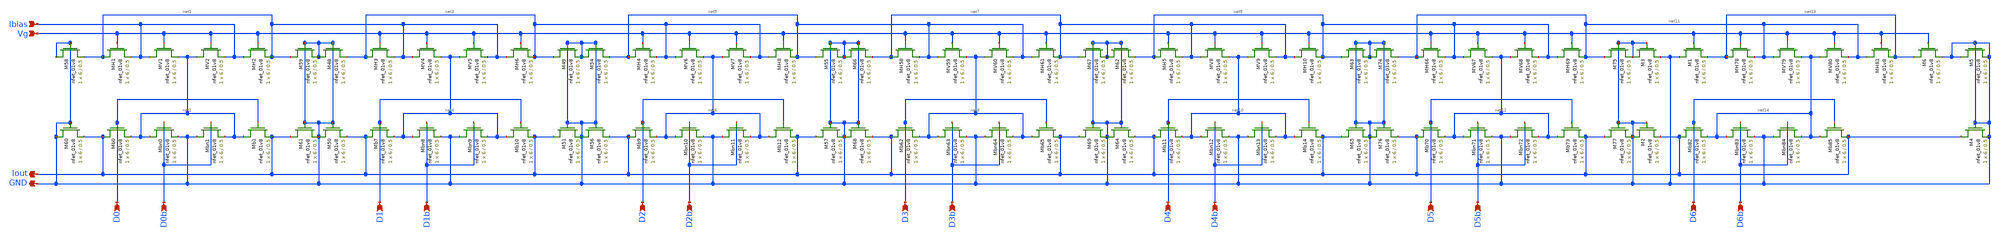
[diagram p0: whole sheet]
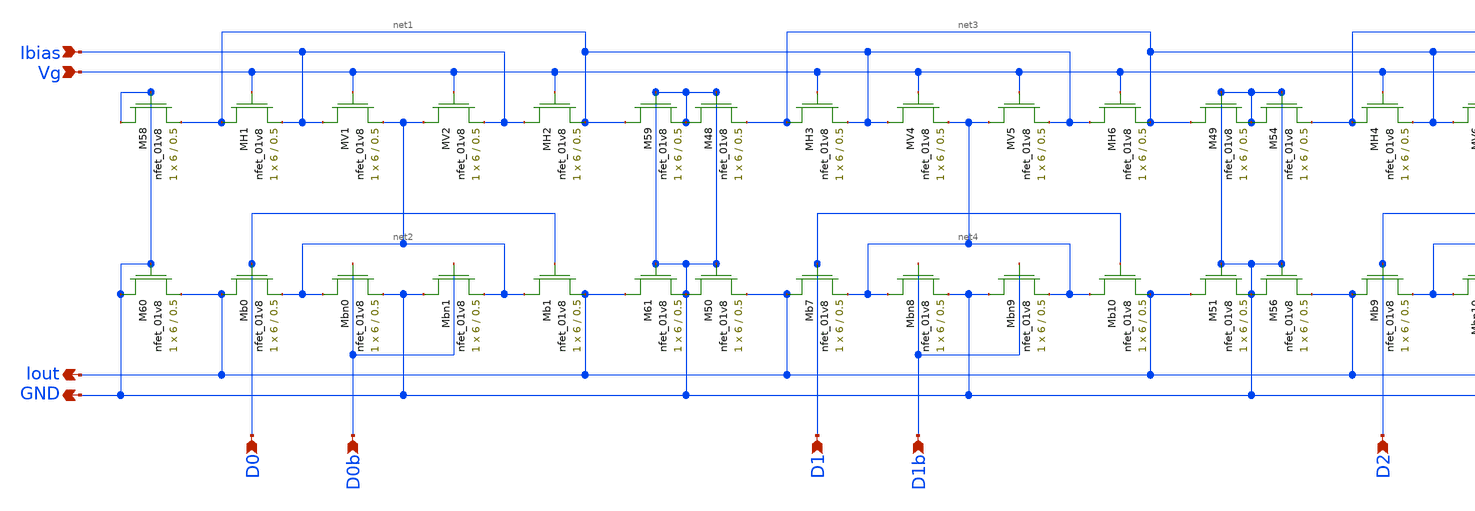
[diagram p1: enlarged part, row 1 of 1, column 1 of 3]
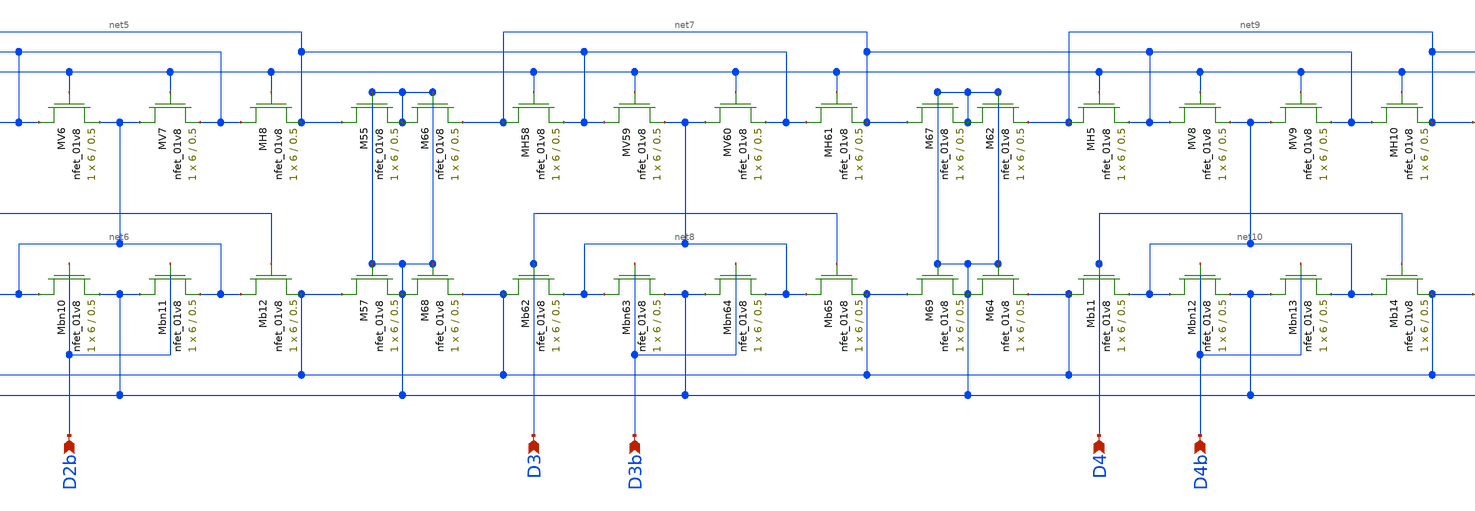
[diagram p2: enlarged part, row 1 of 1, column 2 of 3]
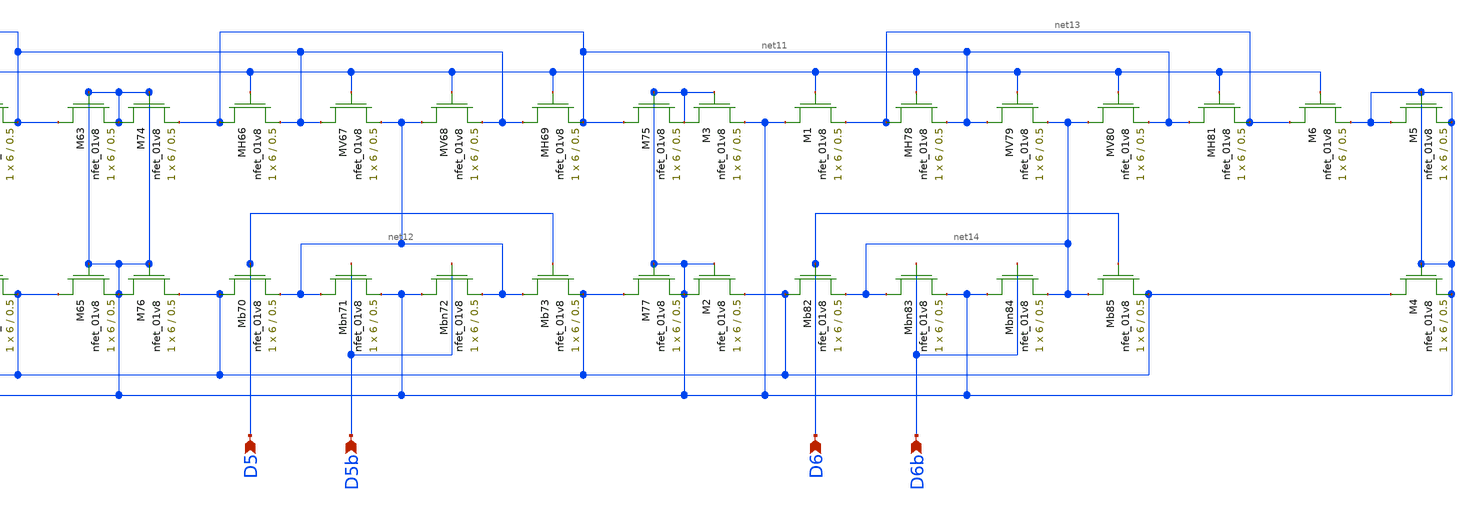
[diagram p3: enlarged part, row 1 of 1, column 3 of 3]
** sch_path: schematics/ieee DAC/Layout_Driven/LDS_ieee_DAC.sch
**.subckt LDS_ieee_DAC D0 D0b GND Iout Vg D1 D1b Ibias D2 D2b D3 D3b D4 D4b D5 D5b D6 D6b
*.ipin D0
*.ipin D0b
*.opin GND
*.opin Iout
*.ipin Vg
*.ipin D1
*.ipin D1b
*.ipin Ibias
*.ipin D2
*.ipin D2b
*.ipin D3
*.ipin D3b
*.ipin D4
*.ipin D4b
*.ipin D5
*.ipin D5b
*.ipin D6
*.ipin D6b
XMH1 net1 Vg Ibias GND sky130_fd_pr__nfet_01v8 L=0.5 W=6 nf=1 ad='int((nf+1)/2) * W/nf * 0.29' as='int((nf+2)/2) * W/nf * 0.29'
+ pd='2*int((nf+1)/2) * (W/nf + 0.29)' ps='2*int((nf+2)/2) * (W/nf + 0.29)' nrd='0.29 / W' nrs='0.29 / W'
+ sa=0 sb=0 sd=0 mult=1 m=1
XMV1 Ibias Vg net2 GND sky130_fd_pr__nfet_01v8 L=0.5 W=6 nf=1 ad='int((nf+1)/2) * W/nf * 0.29' as='int((nf+2)/2) * W/nf * 0.29'
+ pd='2*int((nf+1)/2) * (W/nf + 0.29)' ps='2*int((nf+2)/2) * (W/nf + 0.29)' nrd='0.29 / W' nrs='0.29 / W'
+ sa=0 sb=0 sd=0 mult=1 m=1
XMV2 net2 Vg Ibias GND sky130_fd_pr__nfet_01v8 L=0.5 W=6 nf=1 ad='int((nf+1)/2) * W/nf * 0.29' as='int((nf+2)/2) * W/nf * 0.29'
+ pd='2*int((nf+1)/2) * (W/nf + 0.29)' ps='2*int((nf+2)/2) * (W/nf + 0.29)' nrd='0.29 / W' nrs='0.29 / W'
+ sa=0 sb=0 sd=0 mult=1 m=1
XMH2 Ibias Vg net1 GND sky130_fd_pr__nfet_01v8 L=0.5 W=6 nf=1 ad='int((nf+1)/2) * W/nf * 0.29' as='int((nf+2)/2) * W/nf * 0.29'
+ pd='2*int((nf+1)/2) * (W/nf + 0.29)' ps='2*int((nf+2)/2) * (W/nf + 0.29)' nrd='0.29 / W' nrs='0.29 / W'
+ sa=0 sb=0 sd=0 mult=1 m=1
XMb0 Iout D0 net2 GND sky130_fd_pr__nfet_01v8 L=0.5 W=6 nf=1 ad='int((nf+1)/2) * W/nf * 0.29' as='int((nf+2)/2) * W/nf * 0.29'
+ pd='2*int((nf+1)/2) * (W/nf + 0.29)' ps='2*int((nf+2)/2) * (W/nf + 0.29)' nrd='0.29 / W' nrs='0.29 / W'
+ sa=0 sb=0 sd=0 mult=1 m=1
XMbn0 net2 D0b GND GND sky130_fd_pr__nfet_01v8 L=0.5 W=6 nf=1 ad='int((nf+1)/2) * W/nf * 0.29' as='int((nf+2)/2) * W/nf * 0.29'
+ pd='2*int((nf+1)/2) * (W/nf + 0.29)' ps='2*int((nf+2)/2) * (W/nf + 0.29)' nrd='0.29 / W' nrs='0.29 / W'
+ sa=0 sb=0 sd=0 mult=1 m=1
XMbn1 GND D0b net2 GND sky130_fd_pr__nfet_01v8 L=0.5 W=6 nf=1 ad='int((nf+1)/2) * W/nf * 0.29' as='int((nf+2)/2) * W/nf * 0.29'
+ pd='2*int((nf+1)/2) * (W/nf + 0.29)' ps='2*int((nf+2)/2) * (W/nf + 0.29)' nrd='0.29 / W' nrs='0.29 / W'
+ sa=0 sb=0 sd=0 mult=1 m=1
XMb1 net2 D0 Iout GND sky130_fd_pr__nfet_01v8 L=0.5 W=6 nf=1 ad='int((nf+1)/2) * W/nf * 0.29' as='int((nf+2)/2) * W/nf * 0.29'
+ pd='2*int((nf+1)/2) * (W/nf + 0.29)' ps='2*int((nf+2)/2) * (W/nf + 0.29)' nrd='0.29 / W' nrs='0.29 / W'
+ sa=0 sb=0 sd=0 mult=1 m=1
XM58 GND GND net1 GND sky130_fd_pr__nfet_01v8 L=0.5 W=6 nf=1 ad='int((nf+1)/2) * W/nf * 0.29' as='int((nf+2)/2) * W/nf * 0.29'
+ pd='2*int((nf+1)/2) * (W/nf + 0.29)' ps='2*int((nf+2)/2) * (W/nf + 0.29)' nrd='0.29 / W' nrs='0.29 / W'
+ sa=0 sb=0 sd=0 mult=1 m=1
XM59 net1 GND GND GND sky130_fd_pr__nfet_01v8 L=0.5 W=6 nf=1 ad='int((nf+1)/2) * W/nf * 0.29' as='int((nf+2)/2) * W/nf * 0.29'
+ pd='2*int((nf+1)/2) * (W/nf + 0.29)' ps='2*int((nf+2)/2) * (W/nf + 0.29)' nrd='0.29 / W' nrs='0.29 / W'
+ sa=0 sb=0 sd=0 mult=1 m=1
XM60 GND GND Iout GND sky130_fd_pr__nfet_01v8 L=0.5 W=6 nf=1 ad='int((nf+1)/2) * W/nf * 0.29' as='int((nf+2)/2) * W/nf * 0.29'
+ pd='2*int((nf+1)/2) * (W/nf + 0.29)' ps='2*int((nf+2)/2) * (W/nf + 0.29)' nrd='0.29 / W' nrs='0.29 / W'
+ sa=0 sb=0 sd=0 mult=1 m=1
XM61 Iout GND GND GND sky130_fd_pr__nfet_01v8 L=0.5 W=6 nf=1 ad='int((nf+1)/2) * W/nf * 0.29' as='int((nf+2)/2) * W/nf * 0.29'
+ pd='2*int((nf+1)/2) * (W/nf + 0.29)' ps='2*int((nf+2)/2) * (W/nf + 0.29)' nrd='0.29 / W' nrs='0.29 / W'
+ sa=0 sb=0 sd=0 mult=1 m=1
XMH3 net3 Vg net1 GND sky130_fd_pr__nfet_01v8 L=0.5 W=6 nf=1 ad='int((nf+1)/2) * W/nf * 0.29' as='int((nf+2)/2) * W/nf * 0.29'
+ pd='2*int((nf+1)/2) * (W/nf + 0.29)' ps='2*int((nf+2)/2) * (W/nf + 0.29)' nrd='0.29 / W' nrs='0.29 / W'
+ sa=0 sb=0 sd=0 mult=1 m=1
XMV4 net1 Vg net4 GND sky130_fd_pr__nfet_01v8 L=0.5 W=6 nf=1 ad='int((nf+1)/2) * W/nf * 0.29' as='int((nf+2)/2) * W/nf * 0.29'
+ pd='2*int((nf+1)/2) * (W/nf + 0.29)' ps='2*int((nf+2)/2) * (W/nf + 0.29)' nrd='0.29 / W' nrs='0.29 / W'
+ sa=0 sb=0 sd=0 mult=1 m=1
XMV5 net4 Vg net1 GND sky130_fd_pr__nfet_01v8 L=0.5 W=6 nf=1 ad='int((nf+1)/2) * W/nf * 0.29' as='int((nf+2)/2) * W/nf * 0.29'
+ pd='2*int((nf+1)/2) * (W/nf + 0.29)' ps='2*int((nf+2)/2) * (W/nf + 0.29)' nrd='0.29 / W' nrs='0.29 / W'
+ sa=0 sb=0 sd=0 mult=1 m=1
XMH6 net1 Vg net3 GND sky130_fd_pr__nfet_01v8 L=0.5 W=6 nf=1 ad='int((nf+1)/2) * W/nf * 0.29' as='int((nf+2)/2) * W/nf * 0.29'
+ pd='2*int((nf+1)/2) * (W/nf + 0.29)' ps='2*int((nf+2)/2) * (W/nf + 0.29)' nrd='0.29 / W' nrs='0.29 / W'
+ sa=0 sb=0 sd=0 mult=1 m=1
XMb7 Iout D1 net4 GND sky130_fd_pr__nfet_01v8 L=0.5 W=6 nf=1 ad='int((nf+1)/2) * W/nf * 0.29' as='int((nf+2)/2) * W/nf * 0.29'
+ pd='2*int((nf+1)/2) * (W/nf + 0.29)' ps='2*int((nf+2)/2) * (W/nf + 0.29)' nrd='0.29 / W' nrs='0.29 / W'
+ sa=0 sb=0 sd=0 mult=1 m=1
XMbn8 net4 D1b GND GND sky130_fd_pr__nfet_01v8 L=0.5 W=6 nf=1 ad='int((nf+1)/2) * W/nf * 0.29' as='int((nf+2)/2) * W/nf * 0.29'
+ pd='2*int((nf+1)/2) * (W/nf + 0.29)' ps='2*int((nf+2)/2) * (W/nf + 0.29)' nrd='0.29 / W' nrs='0.29 / W'
+ sa=0 sb=0 sd=0 mult=1 m=1
XMbn9 GND D1b net4 GND sky130_fd_pr__nfet_01v8 L=0.5 W=6 nf=1 ad='int((nf+1)/2) * W/nf * 0.29' as='int((nf+2)/2) * W/nf * 0.29'
+ pd='2*int((nf+1)/2) * (W/nf + 0.29)' ps='2*int((nf+2)/2) * (W/nf + 0.29)' nrd='0.29 / W' nrs='0.29 / W'
+ sa=0 sb=0 sd=0 mult=1 m=1
XMb10 net4 D1 Iout GND sky130_fd_pr__nfet_01v8 L=0.5 W=6 nf=1 ad='int((nf+1)/2) * W/nf * 0.29' as='int((nf+2)/2) * W/nf * 0.29'
+ pd='2*int((nf+1)/2) * (W/nf + 0.29)' ps='2*int((nf+2)/2) * (W/nf + 0.29)' nrd='0.29 / W' nrs='0.29 / W'
+ sa=0 sb=0 sd=0 mult=1 m=1
XM48 GND GND net3 GND sky130_fd_pr__nfet_01v8 L=0.5 W=6 nf=1 ad='int((nf+1)/2) * W/nf * 0.29' as='int((nf+2)/2) * W/nf * 0.29'
+ pd='2*int((nf+1)/2) * (W/nf + 0.29)' ps='2*int((nf+2)/2) * (W/nf + 0.29)' nrd='0.29 / W' nrs='0.29 / W'
+ sa=0 sb=0 sd=0 mult=1 m=1
XM49 net3 GND GND GND sky130_fd_pr__nfet_01v8 L=0.5 W=6 nf=1 ad='int((nf+1)/2) * W/nf * 0.29' as='int((nf+2)/2) * W/nf * 0.29'
+ pd='2*int((nf+1)/2) * (W/nf + 0.29)' ps='2*int((nf+2)/2) * (W/nf + 0.29)' nrd='0.29 / W' nrs='0.29 / W'
+ sa=0 sb=0 sd=0 mult=1 m=1
XM50 GND GND Iout GND sky130_fd_pr__nfet_01v8 L=0.5 W=6 nf=1 ad='int((nf+1)/2) * W/nf * 0.29' as='int((nf+2)/2) * W/nf * 0.29'
+ pd='2*int((nf+1)/2) * (W/nf + 0.29)' ps='2*int((nf+2)/2) * (W/nf + 0.29)' nrd='0.29 / W' nrs='0.29 / W'
+ sa=0 sb=0 sd=0 mult=1 m=1
XM51 Iout GND GND GND sky130_fd_pr__nfet_01v8 L=0.5 W=6 nf=1 ad='int((nf+1)/2) * W/nf * 0.29' as='int((nf+2)/2) * W/nf * 0.29'
+ pd='2*int((nf+1)/2) * (W/nf + 0.29)' ps='2*int((nf+2)/2) * (W/nf + 0.29)' nrd='0.29 / W' nrs='0.29 / W'
+ sa=0 sb=0 sd=0 mult=1 m=1
XMH4 net5 Vg net3 GND sky130_fd_pr__nfet_01v8 L=0.5 W=6 nf=1 ad='int((nf+1)/2) * W/nf * 0.29' as='int((nf+2)/2) * W/nf * 0.29'
+ pd='2*int((nf+1)/2) * (W/nf + 0.29)' ps='2*int((nf+2)/2) * (W/nf + 0.29)' nrd='0.29 / W' nrs='0.29 / W'
+ sa=0 sb=0 sd=0 mult=1 m=1
XMV6 net3 Vg net6 GND sky130_fd_pr__nfet_01v8 L=0.5 W=6 nf=1 ad='int((nf+1)/2) * W/nf * 0.29' as='int((nf+2)/2) * W/nf * 0.29'
+ pd='2*int((nf+1)/2) * (W/nf + 0.29)' ps='2*int((nf+2)/2) * (W/nf + 0.29)' nrd='0.29 / W' nrs='0.29 / W'
+ sa=0 sb=0 sd=0 mult=1 m=1
XMV7 net6 Vg net3 GND sky130_fd_pr__nfet_01v8 L=0.5 W=6 nf=1 ad='int((nf+1)/2) * W/nf * 0.29' as='int((nf+2)/2) * W/nf * 0.29'
+ pd='2*int((nf+1)/2) * (W/nf + 0.29)' ps='2*int((nf+2)/2) * (W/nf + 0.29)' nrd='0.29 / W' nrs='0.29 / W'
+ sa=0 sb=0 sd=0 mult=1 m=1
XMH8 net3 Vg net5 GND sky130_fd_pr__nfet_01v8 L=0.5 W=6 nf=1 ad='int((nf+1)/2) * W/nf * 0.29' as='int((nf+2)/2) * W/nf * 0.29'
+ pd='2*int((nf+1)/2) * (W/nf + 0.29)' ps='2*int((nf+2)/2) * (W/nf + 0.29)' nrd='0.29 / W' nrs='0.29 / W'
+ sa=0 sb=0 sd=0 mult=1 m=1
XMb9 Iout D2 net6 GND sky130_fd_pr__nfet_01v8 L=0.5 W=6 nf=1 ad='int((nf+1)/2) * W/nf * 0.29' as='int((nf+2)/2) * W/nf * 0.29'
+ pd='2*int((nf+1)/2) * (W/nf + 0.29)' ps='2*int((nf+2)/2) * (W/nf + 0.29)' nrd='0.29 / W' nrs='0.29 / W'
+ sa=0 sb=0 sd=0 mult=1 m=1
XMbn10 net6 D2b GND GND sky130_fd_pr__nfet_01v8 L=0.5 W=6 nf=1 ad='int((nf+1)/2) * W/nf * 0.29' as='int((nf+2)/2) * W/nf * 0.29'
+ pd='2*int((nf+1)/2) * (W/nf + 0.29)' ps='2*int((nf+2)/2) * (W/nf + 0.29)' nrd='0.29 / W' nrs='0.29 / W'
+ sa=0 sb=0 sd=0 mult=1 m=1
XMbn11 GND D2b net6 GND sky130_fd_pr__nfet_01v8 L=0.5 W=6 nf=1 ad='int((nf+1)/2) * W/nf * 0.29' as='int((nf+2)/2) * W/nf * 0.29'
+ pd='2*int((nf+1)/2) * (W/nf + 0.29)' ps='2*int((nf+2)/2) * (W/nf + 0.29)' nrd='0.29 / W' nrs='0.29 / W'
+ sa=0 sb=0 sd=0 mult=1 m=1
XMb12 net6 D2 Iout GND sky130_fd_pr__nfet_01v8 L=0.5 W=6 nf=1 ad='int((nf+1)/2) * W/nf * 0.29' as='int((nf+2)/2) * W/nf * 0.29'
+ pd='2*int((nf+1)/2) * (W/nf + 0.29)' ps='2*int((nf+2)/2) * (W/nf + 0.29)' nrd='0.29 / W' nrs='0.29 / W'
+ sa=0 sb=0 sd=0 mult=1 m=1
XM54 GND GND net5 GND sky130_fd_pr__nfet_01v8 L=0.5 W=6 nf=1 ad='int((nf+1)/2) * W/nf * 0.29' as='int((nf+2)/2) * W/nf * 0.29'
+ pd='2*int((nf+1)/2) * (W/nf + 0.29)' ps='2*int((nf+2)/2) * (W/nf + 0.29)' nrd='0.29 / W' nrs='0.29 / W'
+ sa=0 sb=0 sd=0 mult=1 m=1
XM55 net5 GND GND GND sky130_fd_pr__nfet_01v8 L=0.5 W=6 nf=1 ad='int((nf+1)/2) * W/nf * 0.29' as='int((nf+2)/2) * W/nf * 0.29'
+ pd='2*int((nf+1)/2) * (W/nf + 0.29)' ps='2*int((nf+2)/2) * (W/nf + 0.29)' nrd='0.29 / W' nrs='0.29 / W'
+ sa=0 sb=0 sd=0 mult=1 m=1
XM56 GND GND Iout GND sky130_fd_pr__nfet_01v8 L=0.5 W=6 nf=1 ad='int((nf+1)/2) * W/nf * 0.29' as='int((nf+2)/2) * W/nf * 0.29'
+ pd='2*int((nf+1)/2) * (W/nf + 0.29)' ps='2*int((nf+2)/2) * (W/nf + 0.29)' nrd='0.29 / W' nrs='0.29 / W'
+ sa=0 sb=0 sd=0 mult=1 m=1
XM57 Iout GND GND GND sky130_fd_pr__nfet_01v8 L=0.5 W=6 nf=1 ad='int((nf+1)/2) * W/nf * 0.29' as='int((nf+2)/2) * W/nf * 0.29'
+ pd='2*int((nf+1)/2) * (W/nf + 0.29)' ps='2*int((nf+2)/2) * (W/nf + 0.29)' nrd='0.29 / W' nrs='0.29 / W'
+ sa=0 sb=0 sd=0 mult=1 m=1
XMH58 net7 Vg net5 GND sky130_fd_pr__nfet_01v8 L=0.5 W=6 nf=1 ad='int((nf+1)/2) * W/nf * 0.29' as='int((nf+2)/2) * W/nf * 0.29'
+ pd='2*int((nf+1)/2) * (W/nf + 0.29)' ps='2*int((nf+2)/2) * (W/nf + 0.29)' nrd='0.29 / W' nrs='0.29 / W'
+ sa=0 sb=0 sd=0 mult=1 m=1
XMV59 net5 Vg net8 GND sky130_fd_pr__nfet_01v8 L=0.5 W=6 nf=1 ad='int((nf+1)/2) * W/nf * 0.29' as='int((nf+2)/2) * W/nf * 0.29'
+ pd='2*int((nf+1)/2) * (W/nf + 0.29)' ps='2*int((nf+2)/2) * (W/nf + 0.29)' nrd='0.29 / W' nrs='0.29 / W'
+ sa=0 sb=0 sd=0 mult=1 m=1
XMV60 net8 Vg net5 GND sky130_fd_pr__nfet_01v8 L=0.5 W=6 nf=1 ad='int((nf+1)/2) * W/nf * 0.29' as='int((nf+2)/2) * W/nf * 0.29'
+ pd='2*int((nf+1)/2) * (W/nf + 0.29)' ps='2*int((nf+2)/2) * (W/nf + 0.29)' nrd='0.29 / W' nrs='0.29 / W'
+ sa=0 sb=0 sd=0 mult=1 m=1
XMH61 net5 Vg net7 GND sky130_fd_pr__nfet_01v8 L=0.5 W=6 nf=1 ad='int((nf+1)/2) * W/nf * 0.29' as='int((nf+2)/2) * W/nf * 0.29'
+ pd='2*int((nf+1)/2) * (W/nf + 0.29)' ps='2*int((nf+2)/2) * (W/nf + 0.29)' nrd='0.29 / W' nrs='0.29 / W'
+ sa=0 sb=0 sd=0 mult=1 m=1
XMb62 Iout D3 net8 GND sky130_fd_pr__nfet_01v8 L=0.5 W=6 nf=1 ad='int((nf+1)/2) * W/nf * 0.29' as='int((nf+2)/2) * W/nf * 0.29'
+ pd='2*int((nf+1)/2) * (W/nf + 0.29)' ps='2*int((nf+2)/2) * (W/nf + 0.29)' nrd='0.29 / W' nrs='0.29 / W'
+ sa=0 sb=0 sd=0 mult=1 m=1
XMbn63 net8 D3b GND GND sky130_fd_pr__nfet_01v8 L=0.5 W=6 nf=1 ad='int((nf+1)/2) * W/nf * 0.29' as='int((nf+2)/2) * W/nf * 0.29'
+ pd='2*int((nf+1)/2) * (W/nf + 0.29)' ps='2*int((nf+2)/2) * (W/nf + 0.29)' nrd='0.29 / W' nrs='0.29 / W'
+ sa=0 sb=0 sd=0 mult=1 m=1
XMbn64 GND D3b net8 GND sky130_fd_pr__nfet_01v8 L=0.5 W=6 nf=1 ad='int((nf+1)/2) * W/nf * 0.29' as='int((nf+2)/2) * W/nf * 0.29'
+ pd='2*int((nf+1)/2) * (W/nf + 0.29)' ps='2*int((nf+2)/2) * (W/nf + 0.29)' nrd='0.29 / W' nrs='0.29 / W'
+ sa=0 sb=0 sd=0 mult=1 m=1
XMb65 net8 D3 Iout GND sky130_fd_pr__nfet_01v8 L=0.5 W=6 nf=1 ad='int((nf+1)/2) * W/nf * 0.29' as='int((nf+2)/2) * W/nf * 0.29'
+ pd='2*int((nf+1)/2) * (W/nf + 0.29)' ps='2*int((nf+2)/2) * (W/nf + 0.29)' nrd='0.29 / W' nrs='0.29 / W'
+ sa=0 sb=0 sd=0 mult=1 m=1
XM66 GND GND net7 GND sky130_fd_pr__nfet_01v8 L=0.5 W=6 nf=1 ad='int((nf+1)/2) * W/nf * 0.29' as='int((nf+2)/2) * W/nf * 0.29'
+ pd='2*int((nf+1)/2) * (W/nf + 0.29)' ps='2*int((nf+2)/2) * (W/nf + 0.29)' nrd='0.29 / W' nrs='0.29 / W'
+ sa=0 sb=0 sd=0 mult=1 m=1
XM67 net7 GND GND GND sky130_fd_pr__nfet_01v8 L=0.5 W=6 nf=1 ad='int((nf+1)/2) * W/nf * 0.29' as='int((nf+2)/2) * W/nf * 0.29'
+ pd='2*int((nf+1)/2) * (W/nf + 0.29)' ps='2*int((nf+2)/2) * (W/nf + 0.29)' nrd='0.29 / W' nrs='0.29 / W'
+ sa=0 sb=0 sd=0 mult=1 m=1
XM68 GND GND Iout GND sky130_fd_pr__nfet_01v8 L=0.5 W=6 nf=1 ad='int((nf+1)/2) * W/nf * 0.29' as='int((nf+2)/2) * W/nf * 0.29'
+ pd='2*int((nf+1)/2) * (W/nf + 0.29)' ps='2*int((nf+2)/2) * (W/nf + 0.29)' nrd='0.29 / W' nrs='0.29 / W'
+ sa=0 sb=0 sd=0 mult=1 m=1
XM69 Iout GND GND GND sky130_fd_pr__nfet_01v8 L=0.5 W=6 nf=1 ad='int((nf+1)/2) * W/nf * 0.29' as='int((nf+2)/2) * W/nf * 0.29'
+ pd='2*int((nf+1)/2) * (W/nf + 0.29)' ps='2*int((nf+2)/2) * (W/nf + 0.29)' nrd='0.29 / W' nrs='0.29 / W'
+ sa=0 sb=0 sd=0 mult=1 m=1
XMH5 net9 Vg net7 GND sky130_fd_pr__nfet_01v8 L=0.5 W=6 nf=1 ad='int((nf+1)/2) * W/nf * 0.29' as='int((nf+2)/2) * W/nf * 0.29'
+ pd='2*int((nf+1)/2) * (W/nf + 0.29)' ps='2*int((nf+2)/2) * (W/nf + 0.29)' nrd='0.29 / W' nrs='0.29 / W'
+ sa=0 sb=0 sd=0 mult=1 m=1
XMV8 net7 Vg net10 GND sky130_fd_pr__nfet_01v8 L=0.5 W=6 nf=1 ad='int((nf+1)/2) * W/nf * 0.29' as='int((nf+2)/2) * W/nf * 0.29'
+ pd='2*int((nf+1)/2) * (W/nf + 0.29)' ps='2*int((nf+2)/2) * (W/nf + 0.29)' nrd='0.29 / W' nrs='0.29 / W'
+ sa=0 sb=0 sd=0 mult=1 m=1
XMV9 net10 Vg net7 GND sky130_fd_pr__nfet_01v8 L=0.5 W=6 nf=1 ad='int((nf+1)/2) * W/nf * 0.29' as='int((nf+2)/2) * W/nf * 0.29'
+ pd='2*int((nf+1)/2) * (W/nf + 0.29)' ps='2*int((nf+2)/2) * (W/nf + 0.29)' nrd='0.29 / W' nrs='0.29 / W'
+ sa=0 sb=0 sd=0 mult=1 m=1
XMH10 net7 Vg net9 GND sky130_fd_pr__nfet_01v8 L=0.5 W=6 nf=1 ad='int((nf+1)/2) * W/nf * 0.29' as='int((nf+2)/2) * W/nf * 0.29'
+ pd='2*int((nf+1)/2) * (W/nf + 0.29)' ps='2*int((nf+2)/2) * (W/nf + 0.29)' nrd='0.29 / W' nrs='0.29 / W'
+ sa=0 sb=0 sd=0 mult=1 m=1
XMb11 Iout D4 net10 GND sky130_fd_pr__nfet_01v8 L=0.5 W=6 nf=1 ad='int((nf+1)/2) * W/nf * 0.29' as='int((nf+2)/2) * W/nf * 0.29'
+ pd='2*int((nf+1)/2) * (W/nf + 0.29)' ps='2*int((nf+2)/2) * (W/nf + 0.29)' nrd='0.29 / W' nrs='0.29 / W'
+ sa=0 sb=0 sd=0 mult=1 m=1
XMbn12 net10 D4b GND GND sky130_fd_pr__nfet_01v8 L=0.5 W=6 nf=1 ad='int((nf+1)/2) * W/nf * 0.29' as='int((nf+2)/2) * W/nf * 0.29'
+ pd='2*int((nf+1)/2) * (W/nf + 0.29)' ps='2*int((nf+2)/2) * (W/nf + 0.29)' nrd='0.29 / W' nrs='0.29 / W'
+ sa=0 sb=0 sd=0 mult=1 m=1
XMbn13 GND D4b net10 GND sky130_fd_pr__nfet_01v8 L=0.5 W=6 nf=1 ad='int((nf+1)/2) * W/nf * 0.29' as='int((nf+2)/2) * W/nf * 0.29'
+ pd='2*int((nf+1)/2) * (W/nf + 0.29)' ps='2*int((nf+2)/2) * (W/nf + 0.29)' nrd='0.29 / W' nrs='0.29 / W'
+ sa=0 sb=0 sd=0 mult=1 m=1
XMb14 net10 D4 Iout GND sky130_fd_pr__nfet_01v8 L=0.5 W=6 nf=1 ad='int((nf+1)/2) * W/nf * 0.29' as='int((nf+2)/2) * W/nf * 0.29'
+ pd='2*int((nf+1)/2) * (W/nf + 0.29)' ps='2*int((nf+2)/2) * (W/nf + 0.29)' nrd='0.29 / W' nrs='0.29 / W'
+ sa=0 sb=0 sd=0 mult=1 m=1
XM62 GND GND net9 GND sky130_fd_pr__nfet_01v8 L=0.5 W=6 nf=1 ad='int((nf+1)/2) * W/nf * 0.29' as='int((nf+2)/2) * W/nf * 0.29'
+ pd='2*int((nf+1)/2) * (W/nf + 0.29)' ps='2*int((nf+2)/2) * (W/nf + 0.29)' nrd='0.29 / W' nrs='0.29 / W'
+ sa=0 sb=0 sd=0 mult=1 m=1
XM63 net9 GND GND GND sky130_fd_pr__nfet_01v8 L=0.5 W=6 nf=1 ad='int((nf+1)/2) * W/nf * 0.29' as='int((nf+2)/2) * W/nf * 0.29'
+ pd='2*int((nf+1)/2) * (W/nf + 0.29)' ps='2*int((nf+2)/2) * (W/nf + 0.29)' nrd='0.29 / W' nrs='0.29 / W'
+ sa=0 sb=0 sd=0 mult=1 m=1
XM64 GND GND Iout GND sky130_fd_pr__nfet_01v8 L=0.5 W=6 nf=1 ad='int((nf+1)/2) * W/nf * 0.29' as='int((nf+2)/2) * W/nf * 0.29'
+ pd='2*int((nf+1)/2) * (W/nf + 0.29)' ps='2*int((nf+2)/2) * (W/nf + 0.29)' nrd='0.29 / W' nrs='0.29 / W'
+ sa=0 sb=0 sd=0 mult=1 m=1
XM65 Iout GND GND GND sky130_fd_pr__nfet_01v8 L=0.5 W=6 nf=1 ad='int((nf+1)/2) * W/nf * 0.29' as='int((nf+2)/2) * W/nf * 0.29'
+ pd='2*int((nf+1)/2) * (W/nf + 0.29)' ps='2*int((nf+2)/2) * (W/nf + 0.29)' nrd='0.29 / W' nrs='0.29 / W'
+ sa=0 sb=0 sd=0 mult=1 m=1
XMH66 net11 Vg net9 GND sky130_fd_pr__nfet_01v8 L=0.5 W=6 nf=1 ad='int((nf+1)/2) * W/nf * 0.29' as='int((nf+2)/2) * W/nf * 0.29'
+ pd='2*int((nf+1)/2) * (W/nf + 0.29)' ps='2*int((nf+2)/2) * (W/nf + 0.29)' nrd='0.29 / W' nrs='0.29 / W'
+ sa=0 sb=0 sd=0 mult=1 m=1
XMV67 net9 Vg net12 GND sky130_fd_pr__nfet_01v8 L=0.5 W=6 nf=1 ad='int((nf+1)/2) * W/nf * 0.29' as='int((nf+2)/2) * W/nf * 0.29'
+ pd='2*int((nf+1)/2) * (W/nf + 0.29)' ps='2*int((nf+2)/2) * (W/nf + 0.29)' nrd='0.29 / W' nrs='0.29 / W'
+ sa=0 sb=0 sd=0 mult=1 m=1
XMV68 net12 Vg net9 GND sky130_fd_pr__nfet_01v8 L=0.5 W=6 nf=1 ad='int((nf+1)/2) * W/nf * 0.29' as='int((nf+2)/2) * W/nf * 0.29'
+ pd='2*int((nf+1)/2) * (W/nf + 0.29)' ps='2*int((nf+2)/2) * (W/nf + 0.29)' nrd='0.29 / W' nrs='0.29 / W'
+ sa=0 sb=0 sd=0 mult=1 m=1
XMH69 net9 Vg net11 GND sky130_fd_pr__nfet_01v8 L=0.5 W=6 nf=1 ad='int((nf+1)/2) * W/nf * 0.29' as='int((nf+2)/2) * W/nf * 0.29'
+ pd='2*int((nf+1)/2) * (W/nf + 0.29)' ps='2*int((nf+2)/2) * (W/nf + 0.29)' nrd='0.29 / W' nrs='0.29 / W'
+ sa=0 sb=0 sd=0 mult=1 m=1
XMb70 Iout D5 net12 GND sky130_fd_pr__nfet_01v8 L=0.5 W=6 nf=1 ad='int((nf+1)/2) * W/nf * 0.29' as='int((nf+2)/2) * W/nf * 0.29'
+ pd='2*int((nf+1)/2) * (W/nf + 0.29)' ps='2*int((nf+2)/2) * (W/nf + 0.29)' nrd='0.29 / W' nrs='0.29 / W'
+ sa=0 sb=0 sd=0 mult=1 m=1
XMbn71 net12 D5b GND GND sky130_fd_pr__nfet_01v8 L=0.5 W=6 nf=1 ad='int((nf+1)/2) * W/nf * 0.29' as='int((nf+2)/2) * W/nf * 0.29'
+ pd='2*int((nf+1)/2) * (W/nf + 0.29)' ps='2*int((nf+2)/2) * (W/nf + 0.29)' nrd='0.29 / W' nrs='0.29 / W'
+ sa=0 sb=0 sd=0 mult=1 m=1
XMbn72 GND D5b net12 GND sky130_fd_pr__nfet_01v8 L=0.5 W=6 nf=1 ad='int((nf+1)/2) * W/nf * 0.29' as='int((nf+2)/2) * W/nf * 0.29'
+ pd='2*int((nf+1)/2) * (W/nf + 0.29)' ps='2*int((nf+2)/2) * (W/nf + 0.29)' nrd='0.29 / W' nrs='0.29 / W'
+ sa=0 sb=0 sd=0 mult=1 m=1
XMb73 net12 D5 Iout GND sky130_fd_pr__nfet_01v8 L=0.5 W=6 nf=1 ad='int((nf+1)/2) * W/nf * 0.29' as='int((nf+2)/2) * W/nf * 0.29'
+ pd='2*int((nf+1)/2) * (W/nf + 0.29)' ps='2*int((nf+2)/2) * (W/nf + 0.29)' nrd='0.29 / W' nrs='0.29 / W'
+ sa=0 sb=0 sd=0 mult=1 m=1
XM74 GND GND net11 GND sky130_fd_pr__nfet_01v8 L=0.5 W=6 nf=1 ad='int((nf+1)/2) * W/nf * 0.29' as='int((nf+2)/2) * W/nf * 0.29'
+ pd='2*int((nf+1)/2) * (W/nf + 0.29)' ps='2*int((nf+2)/2) * (W/nf + 0.29)' nrd='0.29 / W' nrs='0.29 / W'
+ sa=0 sb=0 sd=0 mult=1 m=1
XM75 net11 GND GND GND sky130_fd_pr__nfet_01v8 L=0.5 W=6 nf=1 ad='int((nf+1)/2) * W/nf * 0.29' as='int((nf+2)/2) * W/nf * 0.29'
+ pd='2*int((nf+1)/2) * (W/nf + 0.29)' ps='2*int((nf+2)/2) * (W/nf + 0.29)' nrd='0.29 / W' nrs='0.29 / W'
+ sa=0 sb=0 sd=0 mult=1 m=1
XM76 GND GND Iout GND sky130_fd_pr__nfet_01v8 L=0.5 W=6 nf=1 ad='int((nf+1)/2) * W/nf * 0.29' as='int((nf+2)/2) * W/nf * 0.29'
+ pd='2*int((nf+1)/2) * (W/nf + 0.29)' ps='2*int((nf+2)/2) * (W/nf + 0.29)' nrd='0.29 / W' nrs='0.29 / W'
+ sa=0 sb=0 sd=0 mult=1 m=1
XM77 Iout GND GND GND sky130_fd_pr__nfet_01v8 L=0.5 W=6 nf=1 ad='int((nf+1)/2) * W/nf * 0.29' as='int((nf+2)/2) * W/nf * 0.29'
+ pd='2*int((nf+1)/2) * (W/nf + 0.29)' ps='2*int((nf+2)/2) * (W/nf + 0.29)' nrd='0.29 / W' nrs='0.29 / W'
+ sa=0 sb=0 sd=0 mult=1 m=1
XMH78 net13 Vg net11 GND sky130_fd_pr__nfet_01v8 L=0.5 W=6 nf=1 ad='int((nf+1)/2) * W/nf * 0.29' as='int((nf+2)/2) * W/nf * 0.29'
+ pd='2*int((nf+1)/2) * (W/nf + 0.29)' ps='2*int((nf+2)/2) * (W/nf + 0.29)' nrd='0.29 / W' nrs='0.29 / W'
+ sa=0 sb=0 sd=0 mult=1 m=1
XMV79 net11 Vg net14 GND sky130_fd_pr__nfet_01v8 L=0.5 W=6 nf=1 ad='int((nf+1)/2) * W/nf * 0.29' as='int((nf+2)/2) * W/nf * 0.29'
+ pd='2*int((nf+1)/2) * (W/nf + 0.29)' ps='2*int((nf+2)/2) * (W/nf + 0.29)' nrd='0.29 / W' nrs='0.29 / W'
+ sa=0 sb=0 sd=0 mult=1 m=1
XMV80 net14 Vg net11 GND sky130_fd_pr__nfet_01v8 L=0.5 W=6 nf=1 ad='int((nf+1)/2) * W/nf * 0.29' as='int((nf+2)/2) * W/nf * 0.29'
+ pd='2*int((nf+1)/2) * (W/nf + 0.29)' ps='2*int((nf+2)/2) * (W/nf + 0.29)' nrd='0.29 / W' nrs='0.29 / W'
+ sa=0 sb=0 sd=0 mult=1 m=1
XMH81 net11 Vg net13 GND sky130_fd_pr__nfet_01v8 L=0.5 W=6 nf=1 ad='int((nf+1)/2) * W/nf * 0.29' as='int((nf+2)/2) * W/nf * 0.29'
+ pd='2*int((nf+1)/2) * (W/nf + 0.29)' ps='2*int((nf+2)/2) * (W/nf + 0.29)' nrd='0.29 / W' nrs='0.29 / W'
+ sa=0 sb=0 sd=0 mult=1 m=1
XMb82 Iout D6 net14 GND sky130_fd_pr__nfet_01v8 L=0.5 W=6 nf=1 ad='int((nf+1)/2) * W/nf * 0.29' as='int((nf+2)/2) * W/nf * 0.29'
+ pd='2*int((nf+1)/2) * (W/nf + 0.29)' ps='2*int((nf+2)/2) * (W/nf + 0.29)' nrd='0.29 / W' nrs='0.29 / W'
+ sa=0 sb=0 sd=0 mult=1 m=1
XMbn83 net14 D6b GND GND sky130_fd_pr__nfet_01v8 L=0.5 W=6 nf=1 ad='int((nf+1)/2) * W/nf * 0.29' as='int((nf+2)/2) * W/nf * 0.29'
+ pd='2*int((nf+1)/2) * (W/nf + 0.29)' ps='2*int((nf+2)/2) * (W/nf + 0.29)' nrd='0.29 / W' nrs='0.29 / W'
+ sa=0 sb=0 sd=0 mult=1 m=1
XMbn84 GND D6b net14 GND sky130_fd_pr__nfet_01v8 L=0.5 W=6 nf=1 ad='int((nf+1)/2) * W/nf * 0.29' as='int((nf+2)/2) * W/nf * 0.29'
+ pd='2*int((nf+1)/2) * (W/nf + 0.29)' ps='2*int((nf+2)/2) * (W/nf + 0.29)' nrd='0.29 / W' nrs='0.29 / W'
+ sa=0 sb=0 sd=0 mult=1 m=1
XMb85 net14 D6 Iout GND sky130_fd_pr__nfet_01v8 L=0.5 W=6 nf=1 ad='int((nf+1)/2) * W/nf * 0.29' as='int((nf+2)/2) * W/nf * 0.29'
+ pd='2*int((nf+1)/2) * (W/nf + 0.29)' ps='2*int((nf+2)/2) * (W/nf + 0.29)' nrd='0.29 / W' nrs='0.29 / W'
+ sa=0 sb=0 sd=0 mult=1 m=1
XM1 GND Vg net13 GND sky130_fd_pr__nfet_01v8 L=0.5 W=6 nf=1 ad='int((nf+1)/2) * W/nf * 0.29' as='int((nf+2)/2) * W/nf * 0.29'
+ pd='2*int((nf+1)/2) * (W/nf + 0.29)' ps='2*int((nf+2)/2) * (W/nf + 0.29)' nrd='0.29 / W' nrs='0.29 / W'
+ sa=0 sb=0 sd=0 mult=1 m=1
XM2 GND GND Iout GND sky130_fd_pr__nfet_01v8 L=0.5 W=6 nf=1 ad='int((nf+1)/2) * W/nf * 0.29' as='int((nf+2)/2) * W/nf * 0.29'
+ pd='2*int((nf+1)/2) * (W/nf + 0.29)' ps='2*int((nf+2)/2) * (W/nf + 0.29)' nrd='0.29 / W' nrs='0.29 / W'
+ sa=0 sb=0 sd=0 mult=1 m=1
XM4 Iout GND GND GND sky130_fd_pr__nfet_01v8 L=0.5 W=6 nf=1 ad='int((nf+1)/2) * W/nf * 0.29' as='int((nf+2)/2) * W/nf * 0.29'
+ pd='2*int((nf+1)/2) * (W/nf + 0.29)' ps='2*int((nf+2)/2) * (W/nf + 0.29)' nrd='0.29 / W' nrs='0.29 / W'
+ sa=0 sb=0 sd=0 mult=1 m=1
XM5 GND GND GND GND sky130_fd_pr__nfet_01v8 L=0.5 W=6 nf=1 ad='int((nf+1)/2) * W/nf * 0.29' as='int((nf+2)/2) * W/nf * 0.29'
+ pd='2*int((nf+1)/2) * (W/nf + 0.29)' ps='2*int((nf+2)/2) * (W/nf + 0.29)' nrd='0.29 / W' nrs='0.29 / W'
+ sa=0 sb=0 sd=0 mult=1 m=1
XM6 net13 Vg GND GND sky130_fd_pr__nfet_01v8 L=0.5 W=6 nf=1 ad='int((nf+1)/2) * W/nf * 0.29' as='int((nf+2)/2) * W/nf * 0.29'
+ pd='2*int((nf+1)/2) * (W/nf + 0.29)' ps='2*int((nf+2)/2) * (W/nf + 0.29)' nrd='0.29 / W' nrs='0.29 / W'
+ sa=0 sb=0 sd=0 mult=1 m=1
XM3 GND GND GND GND sky130_fd_pr__nfet_01v8 L=0.5 W=6 nf=1 ad='int((nf+1)/2) * W/nf * 0.29' as='int((nf+2)/2) * W/nf * 0.29'
+ pd='2*int((nf+1)/2) * (W/nf + 0.29)' ps='2*int((nf+2)/2) * (W/nf + 0.29)' nrd='0.29 / W' nrs='0.29 / W'
+ sa=0 sb=0 sd=0 mult=1 m=1
**.ends
.end
